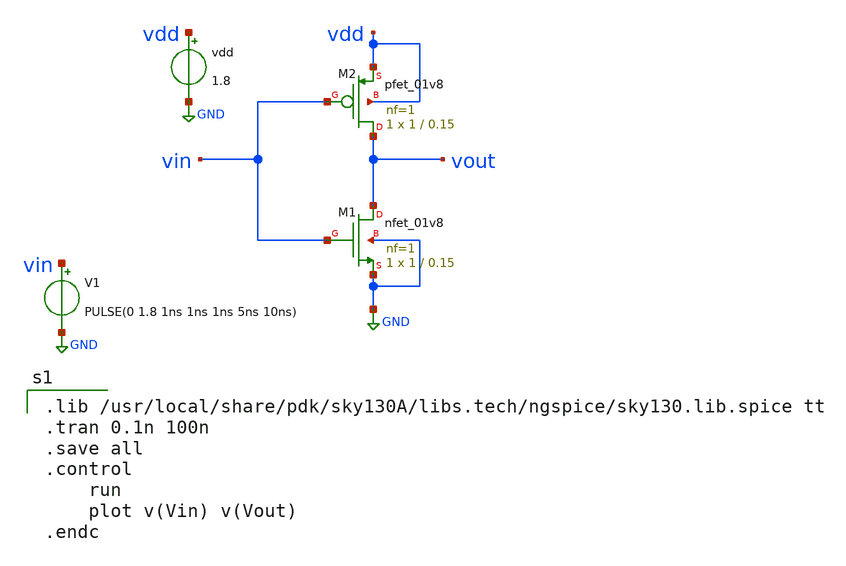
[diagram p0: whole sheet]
** sch_path: CMOS_INVERTER/CMOS_INVERTER.sch
**.subckt CMOS_INVERTER
V1 vin GND PULSE(0 1.8 1ns 1ns 1ns 5ns 10ns)
vdd vdd GND 1.8
XM1 vout vin GND GND sky130_fd_pr__nfet_01v8 L=0.15 W=1 nf=1 ad='int((1 + 1)/2) * 1 / 1 * 0.29' as='int((1 + 2)/2) * 1 / 1 * 0.29'
+ pd='2*int((1 + 1)/2) * (1 / 1 + 0.29)' ps='2*int((1 + 2)/2) * (1 / 1 + 0.29)' nrd='0.29 / 1 ' nrs='0.29 / 1 '
+ sa=0 sb=0 sd=0 mult=1 m=1
XM2 vout vin vdd vdd sky130_fd_pr__pfet_01v8 L=0.15 W=1 nf=1 ad='int((1 + 1)/2) * 1 / 1 * 0.29' as='int((1 + 2)/2) * 1 / 1 * 0.29'
+ pd='2*int((1 + 1)/2) * (1 / 1 + 0.29)' ps='2*int((1 + 2)/2) * (1 / 1 + 0.29)' nrd='0.29 / 1 ' nrs='0.29 / 1 '
+ sa=0 sb=0 sd=0 mult=1 m=1
**** begin user architecture code

.lib /usr/local/share/pdk/sky130A/libs.tech/ngspice/sky130.lib.spice tt
.tran 0.1n 100n
.save all
.control
	run
	plot v(Vin) v(Vout)
.endc

**** end user architecture code
**.ends
.GLOBAL GND
.end
